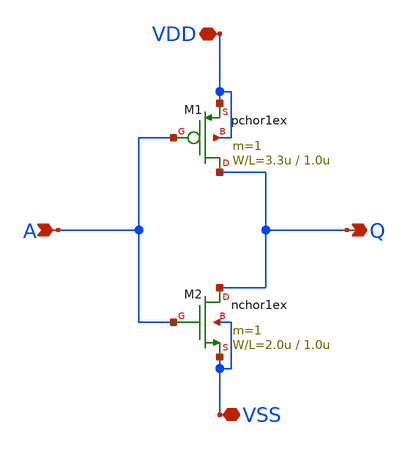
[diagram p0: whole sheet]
** sch_path: samples/inverter/PTS06/inverter.sch
**.subckt inverter A Q VDD VSS
*.ipin A
*.opin Q
*.iopin VDD
*.iopin VSS
M1 Q A VDD VDD pchor1ex L=1.0u W=3.3u m=1
M2 Q A VSS VSS nchor1ex L=1.0u W=2.0u m=1
**.ends
.end
